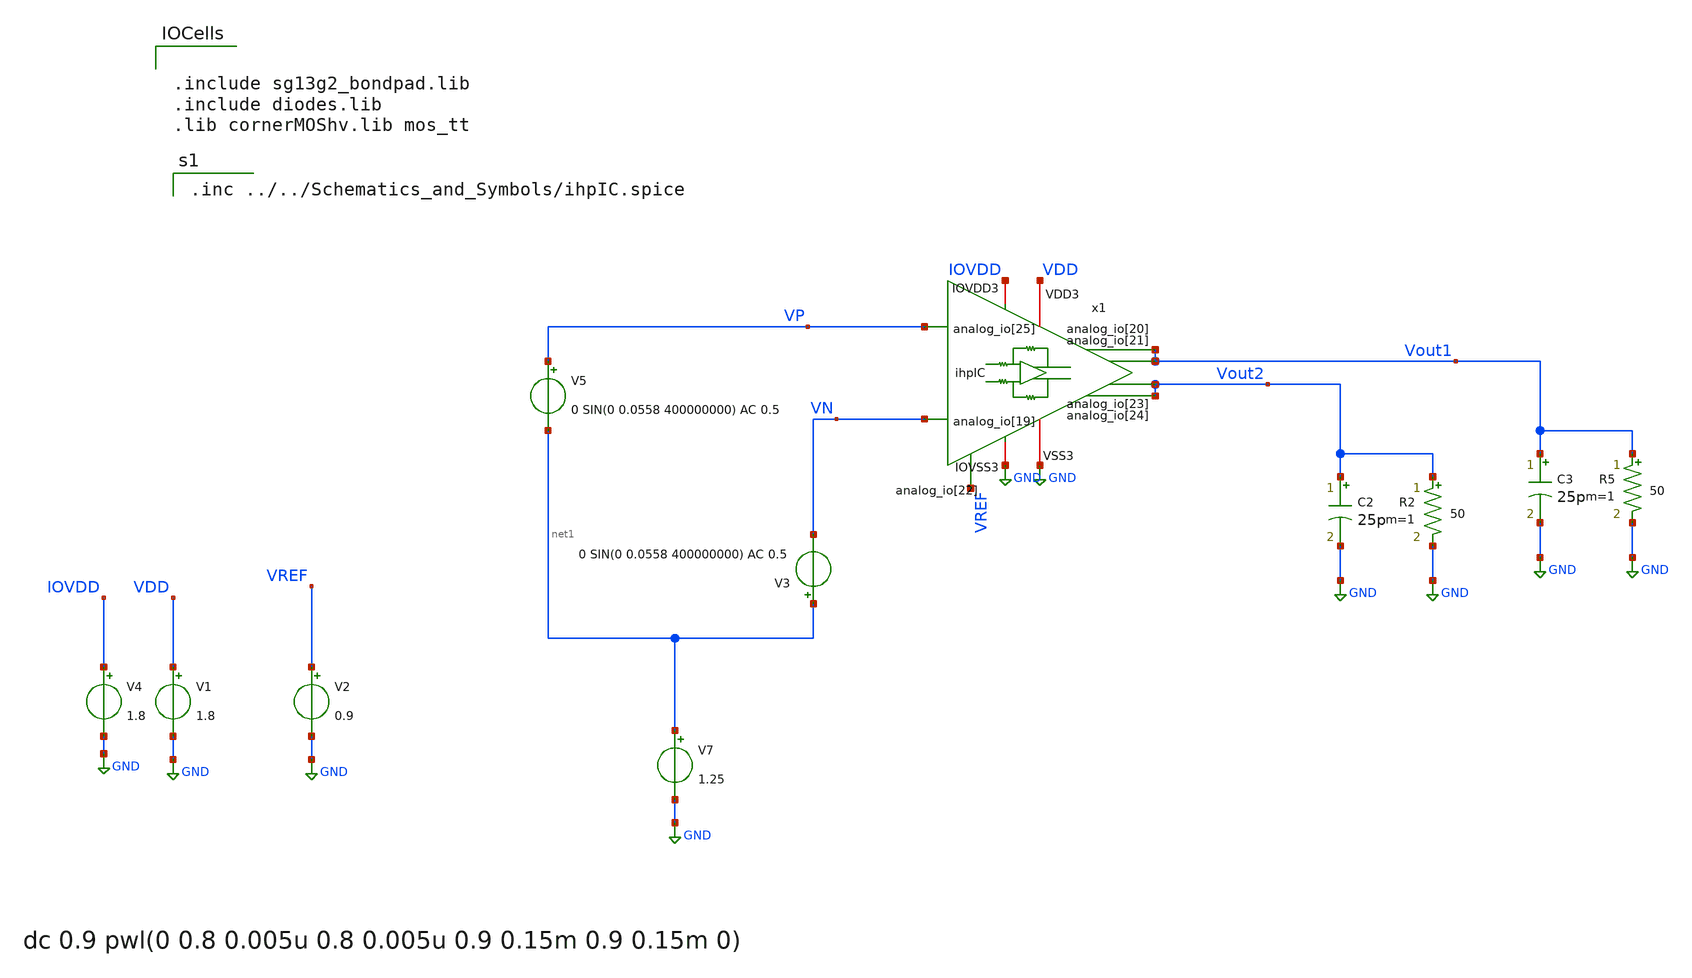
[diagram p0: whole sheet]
** sch_path: OTA_Telescopic_backup/OTA_Telescopic_NO_FLATTEN/Testbenchs/HPA_CL.sch
**.subckt HPA_CL
V7 net1 GND 1.25
V5 VP net1 0 SIN(0 0.0558 400000000) AC 0.5
V1 VDD GND 1.8
V2 VREF GND 0.9
V3 net1 VN 0 SIN(0 0.0558 400000000) AC 0.5
C2 Vout2 GND 25p m=1
R2 Vout2 GND 50 m=1
C3 Vout1 GND 25p m=1
R5 Vout1 GND 50 m=1
x1 VDD VREF Vout2 Vout1 VP VN GND IOVDD GND Vout2 Vout1 ihpIC
V4 IOVDD GND 1.8
**** begin user architecture code

** opencircuitdesign pdks install
.lib cornerMOSlv.lib mos_tt
.lib cornerRES.lib res_typ
.lib cornerCAP.lib cap_typ
.temp 65



.control
 set color0 = white

* AC simulation
ac dec 1000 1 1T
let Av = db(v(Vout1)-v(Vout2))
meas ac Ao FIND Av WHEN frequency=10
let ABW = Ao-3
meas ac BW WHEN Av=ABW
meas ac UGBW WHEN Av=0
let phase_vec = 180/pi*cph(v(Vout1)-v(Vout2))

* Phase margin (PM)
meas ac phase FIND phase_vec WHEN frequency=UGBW
let PM = phase+180
print PM

* Gain margin (GM)
meas ac freq180 FIND frequency WHEN phase_vec=-180
meas ac gain FIND Av WHEN frequency=freq180
let GM = 0-gain

print GM
plot Av
plot phase_vec

write AC_OL.raw
wrdata AvCL_ Av

*DC simulation

op
let vout_dc = v(Vout1)
print vout_dc
write OTA_Telescopic_TOP_TB_CL.raw

.endc



.inc ../../Schematics_and_Symbols/ihpIC.spice



.include sg13g2_bondpad.lib
.include diodes.lib
.lib cornerMOShv.lib mos_tt


**** end user architecture code
**.ends
.GLOBAL GND
.end
